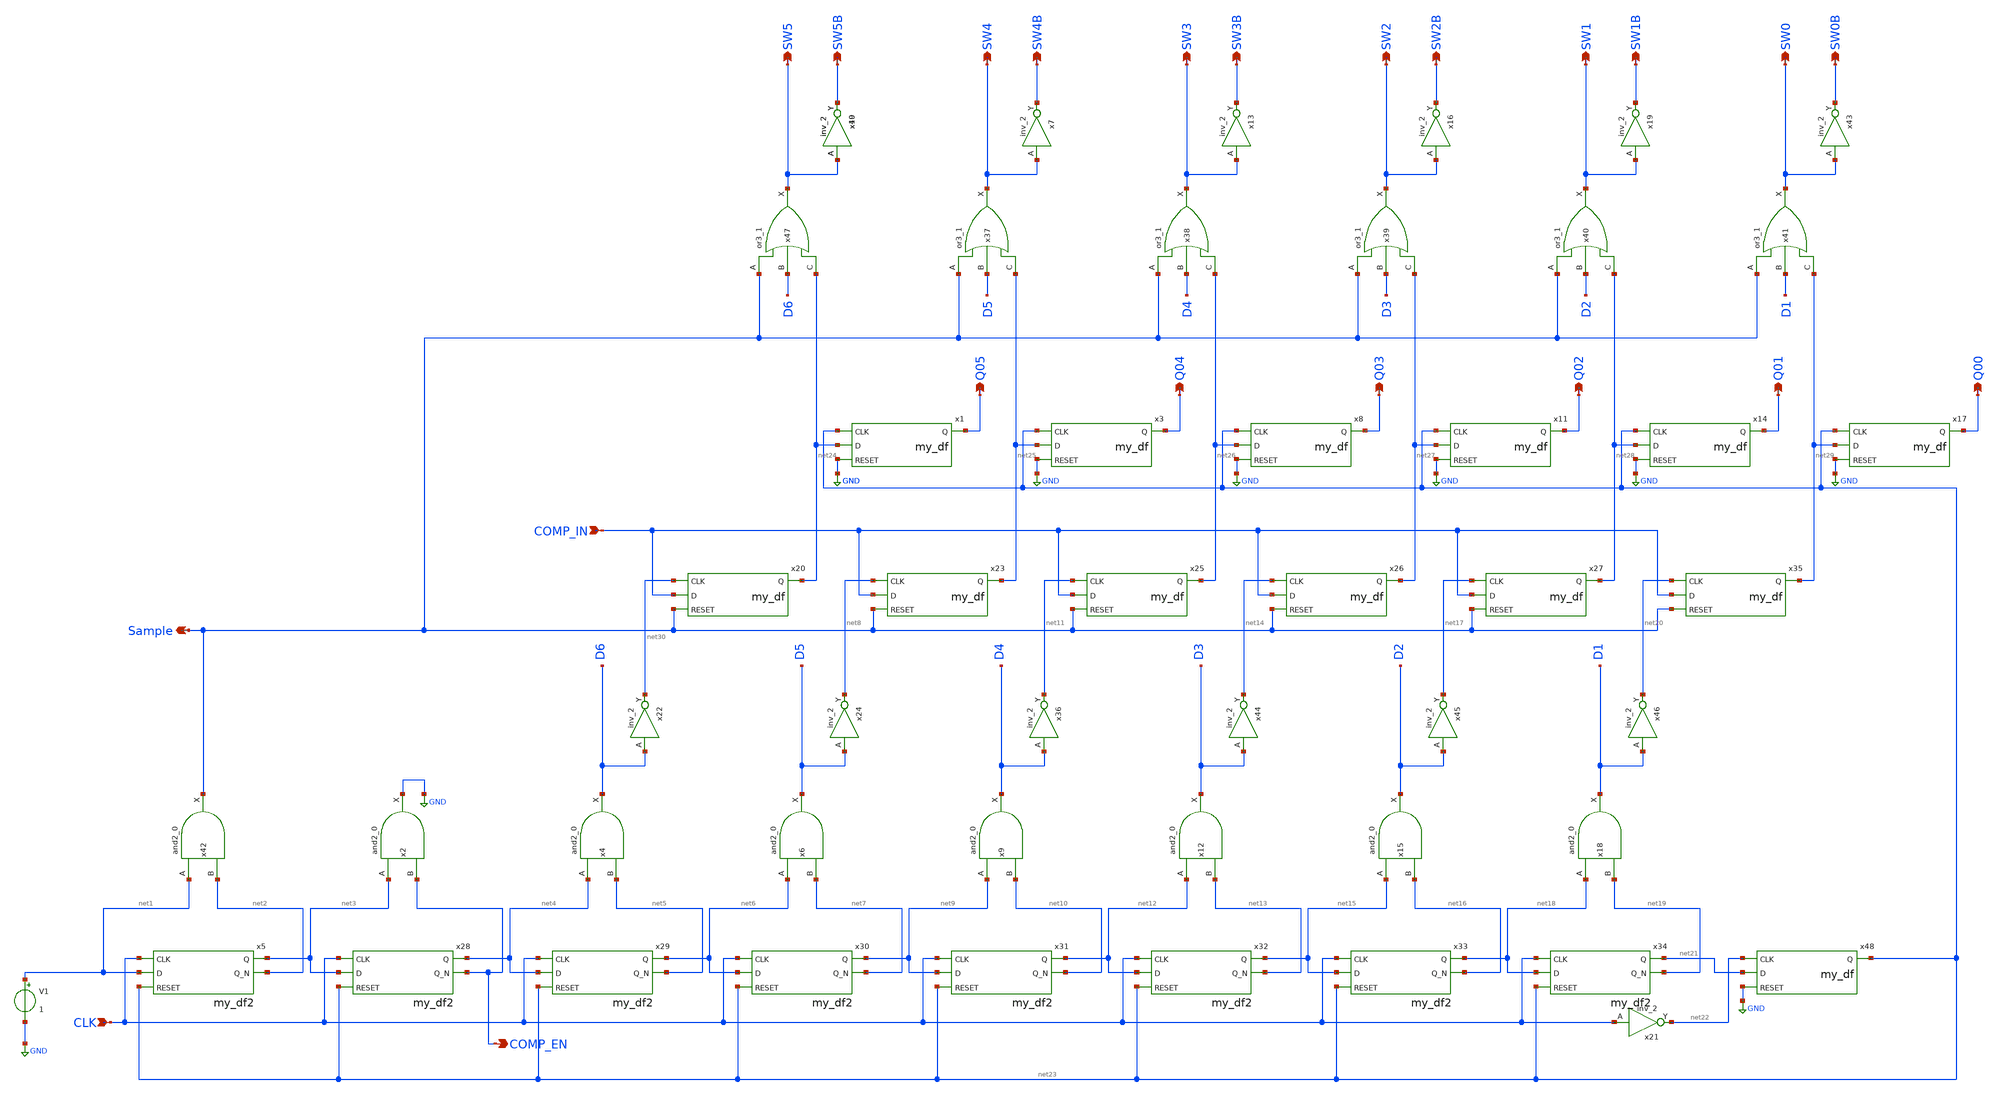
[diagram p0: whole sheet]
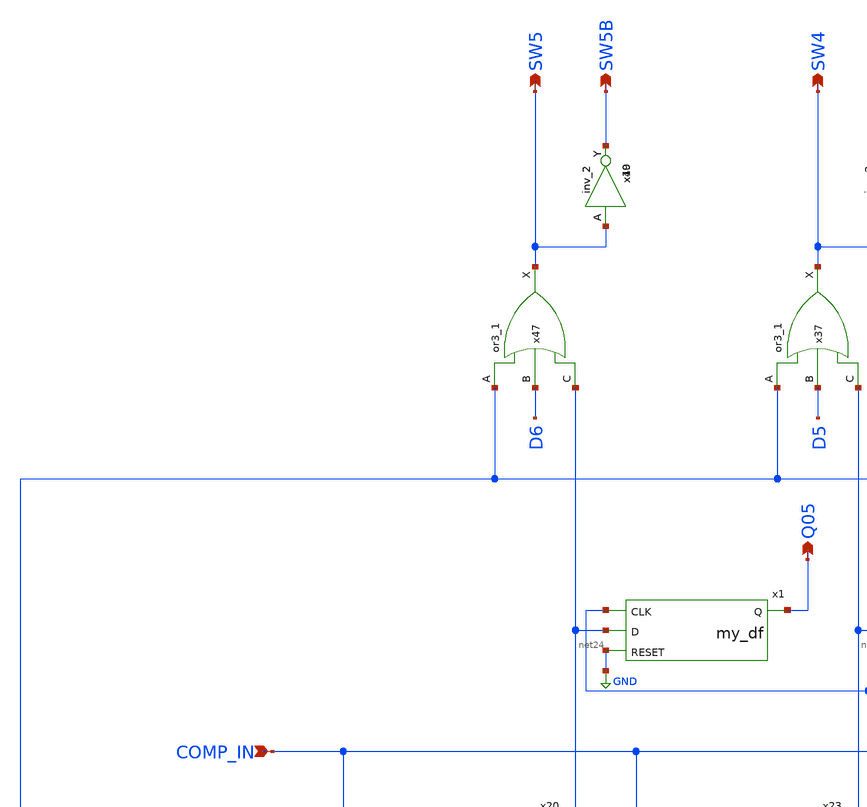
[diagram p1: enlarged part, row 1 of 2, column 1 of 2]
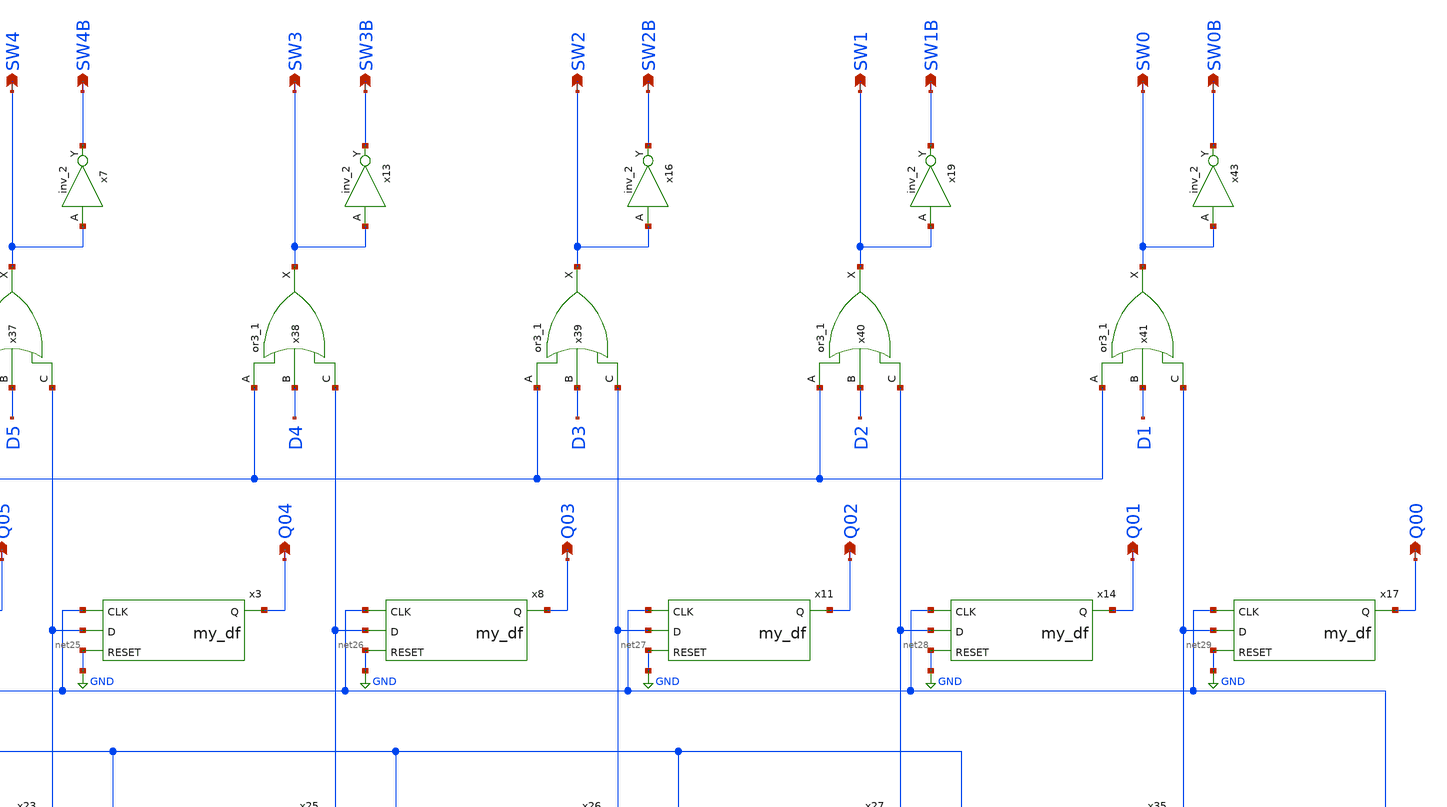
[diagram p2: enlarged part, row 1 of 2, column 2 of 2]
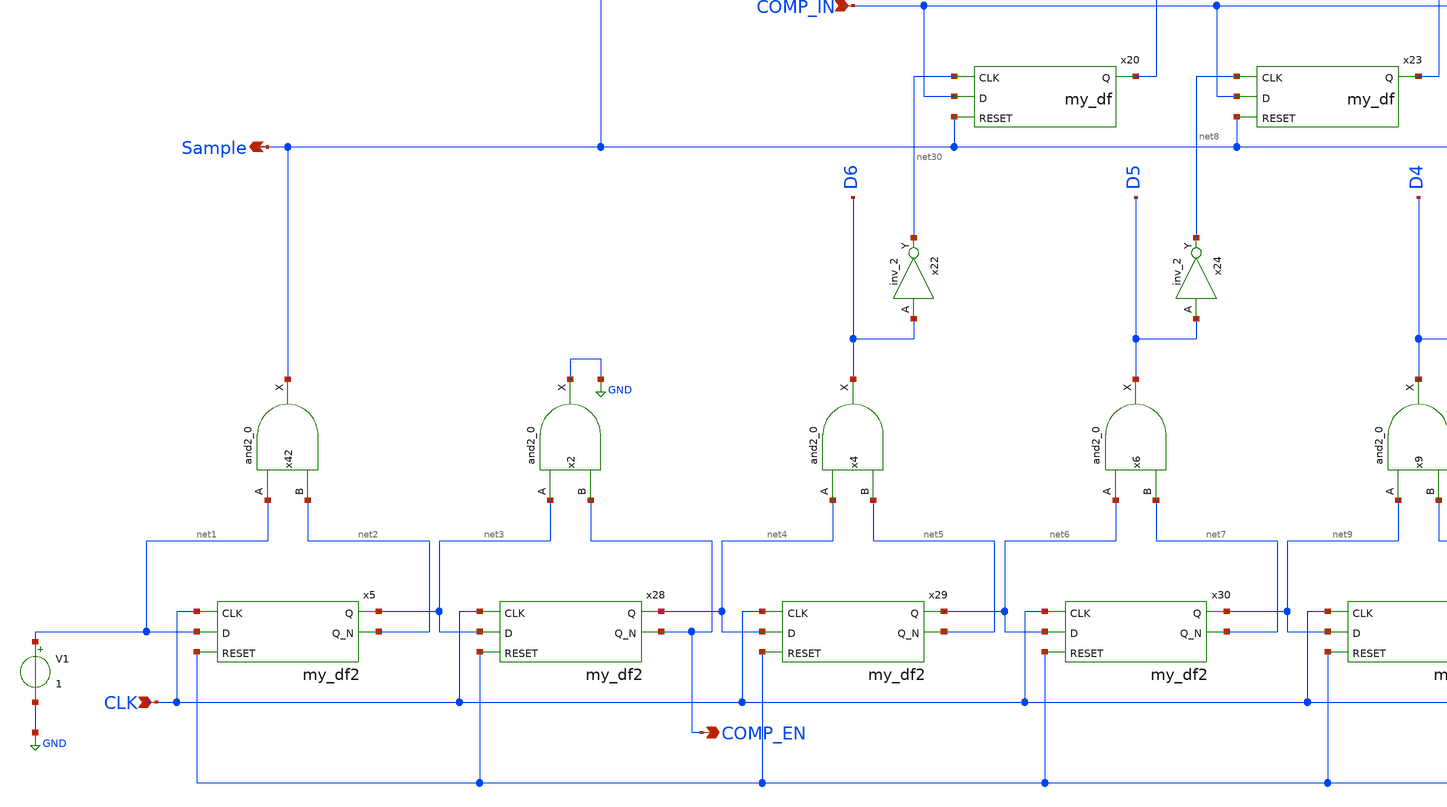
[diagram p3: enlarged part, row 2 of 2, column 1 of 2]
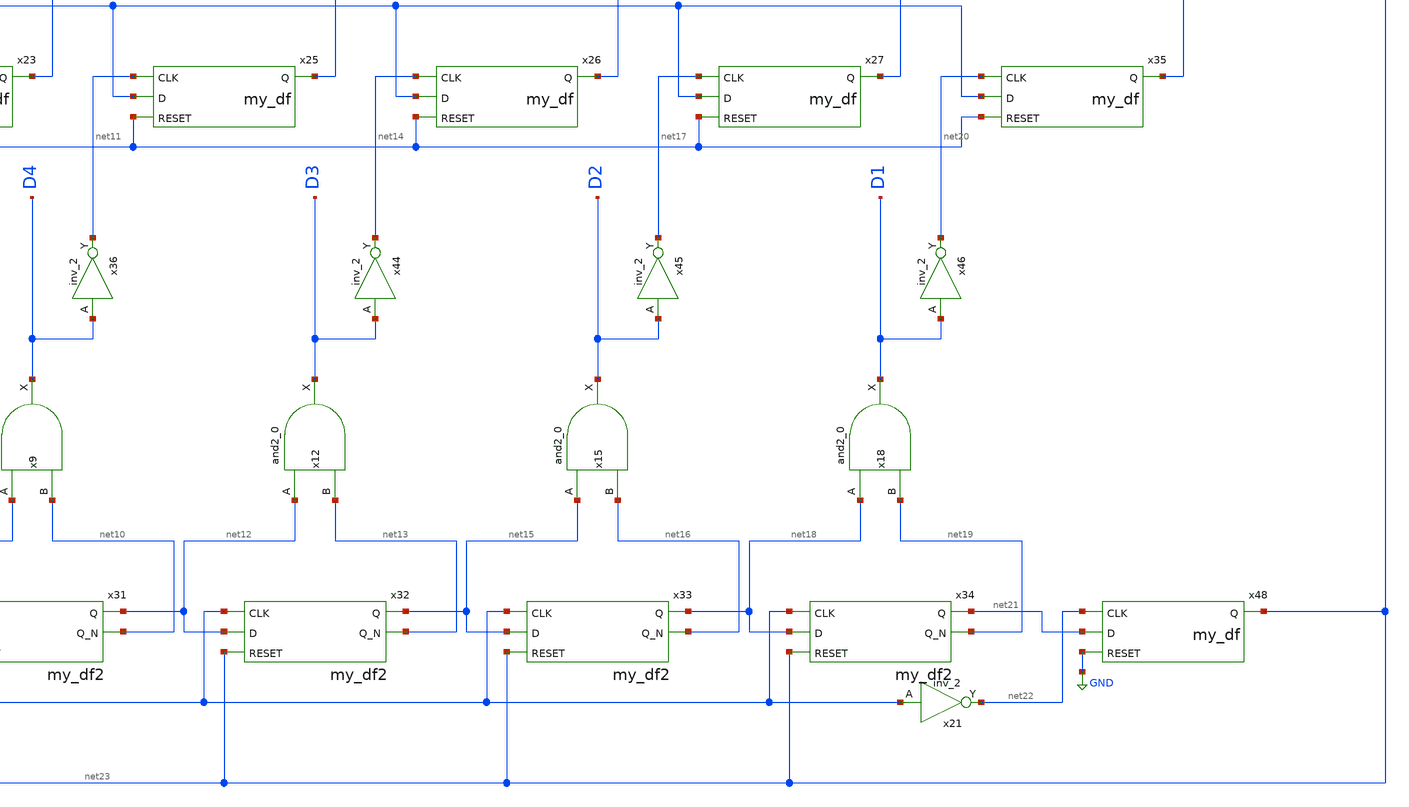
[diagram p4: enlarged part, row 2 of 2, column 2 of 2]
** sch_path: my_sar_logic.sch
**.subckt my_sar_logic CLK COMP_EN Sample COMP_IN Q05 Q04 Q03 Q02 Q01 Q00 SW5 SW5B SW4 SW4B SW3 SW3B
*+ SW2 SW2B SW1 SW1B SW0 SW0B
*.ipin CLK
*.opin COMP_EN
*.opin Sample
*.ipin COMP_IN
*.opin Q05
*.opin Q04
*.opin Q03
*.opin Q02
*.opin Q01
*.opin Q00
*.opin SW5
*.opin SW5B
*.opin SW4
*.opin SW4B
*.opin SW3
*.opin SW3B
*.opin SW2
*.opin SW2B
*.opin SW1
*.opin SW1B
*.opin SW0
*.opin SW0B
V1 net1 GND 1
x49 SW5 GND GND VDD VDD SW5B sky130_fd_sc_hd__inv_2
x7 SW4 GND GND VDD VDD SW4B sky130_fd_sc_hd__inv_2
x10 SW5 GND GND VDD VDD SW5B sky130_fd_sc_hd__inv_2
x13 SW3 GND GND VDD VDD SW3B sky130_fd_sc_hd__inv_2
x16 SW2 GND GND VDD VDD SW2B sky130_fd_sc_hd__inv_2
x19 SW1 GND GND VDD VDD SW1B sky130_fd_sc_hd__inv_2
x43 SW0 GND GND VDD VDD SW0B sky130_fd_sc_hd__inv_2
x22 D6 GND GND VDD VDD net30 sky130_fd_sc_hd__inv_2
x24 D5 GND GND VDD VDD net8 sky130_fd_sc_hd__inv_2
x36 D4 GND GND VDD VDD net11 sky130_fd_sc_hd__inv_2
x44 D3 GND GND VDD VDD net14 sky130_fd_sc_hd__inv_2
x45 D2 GND GND VDD VDD net17 sky130_fd_sc_hd__inv_2
x46 D1 GND GND VDD VDD net20 sky130_fd_sc_hd__inv_2
x47 Sample D6 net24 GND GND VDD VDD SW5 sky130_fd_sc_hd__or3_1
x37 Sample D5 net25 GND GND VDD VDD SW4 sky130_fd_sc_hd__or3_1
x38 Sample D4 net26 GND GND VDD VDD SW3 sky130_fd_sc_hd__or3_1
x39 Sample D3 net27 GND GND VDD VDD SW2 sky130_fd_sc_hd__or3_1
x40 Sample D2 net28 GND GND VDD VDD SW1 sky130_fd_sc_hd__or3_1
x41 Sample D1 net29 GND GND VDD VDD SW0 sky130_fd_sc_hd__or3_1
x42 net1 net2 GND GND VDD VDD Sample sky130_fd_sc_hd__and2_0
x2 net3 COMP_EN GND GND VDD VDD GND sky130_fd_sc_hd__and2_0
x4 net4 net5 GND GND VDD VDD D6 sky130_fd_sc_hd__and2_0
x6 net6 net7 GND GND VDD VDD D5 sky130_fd_sc_hd__and2_0
x9 net9 net10 GND GND VDD VDD D4 sky130_fd_sc_hd__and2_0
x12 net12 net13 GND GND VDD VDD D3 sky130_fd_sc_hd__and2_0
x15 net15 net16 GND GND VDD VDD D2 sky130_fd_sc_hd__and2_0
x18 net18 net19 GND GND VDD VDD D1 sky130_fd_sc_hd__and2_0
x21 CLK GND GND VDD VDD net22 sky130_fd_sc_hd__inv_2
x1 net23 Q05 net24 GND my_df
x3 net23 Q04 net25 GND my_df
x8 net23 Q03 net26 GND my_df
x11 net23 Q02 net27 GND my_df
x14 net23 Q01 net28 GND my_df
x17 net23 Q00 net29 GND my_df
x20 net30 net24 COMP_IN Sample my_df
x23 net8 net25 COMP_IN Sample my_df
x25 net11 net26 COMP_IN Sample my_df
x26 net14 net27 COMP_IN Sample my_df
x27 net17 net28 COMP_IN Sample my_df
x5 CLK net3 net1 net2 net23 my_df2
x28 CLK net4 net3 COMP_EN net23 my_df2
x29 CLK net6 net4 net5 net23 my_df2
x30 CLK net9 net6 net7 net23 my_df2
x31 CLK net12 net9 net10 net23 my_df2
x32 CLK net15 net12 net13 net23 my_df2
x33 CLK net18 net15 net16 net23 my_df2
x34 CLK net21 net18 net19 net23 my_df2
x35 net20 net29 COMP_IN Sample my_df
x48 net22 net23 net21 GND my_df
**.ends
.GLOBAL GND
.end
